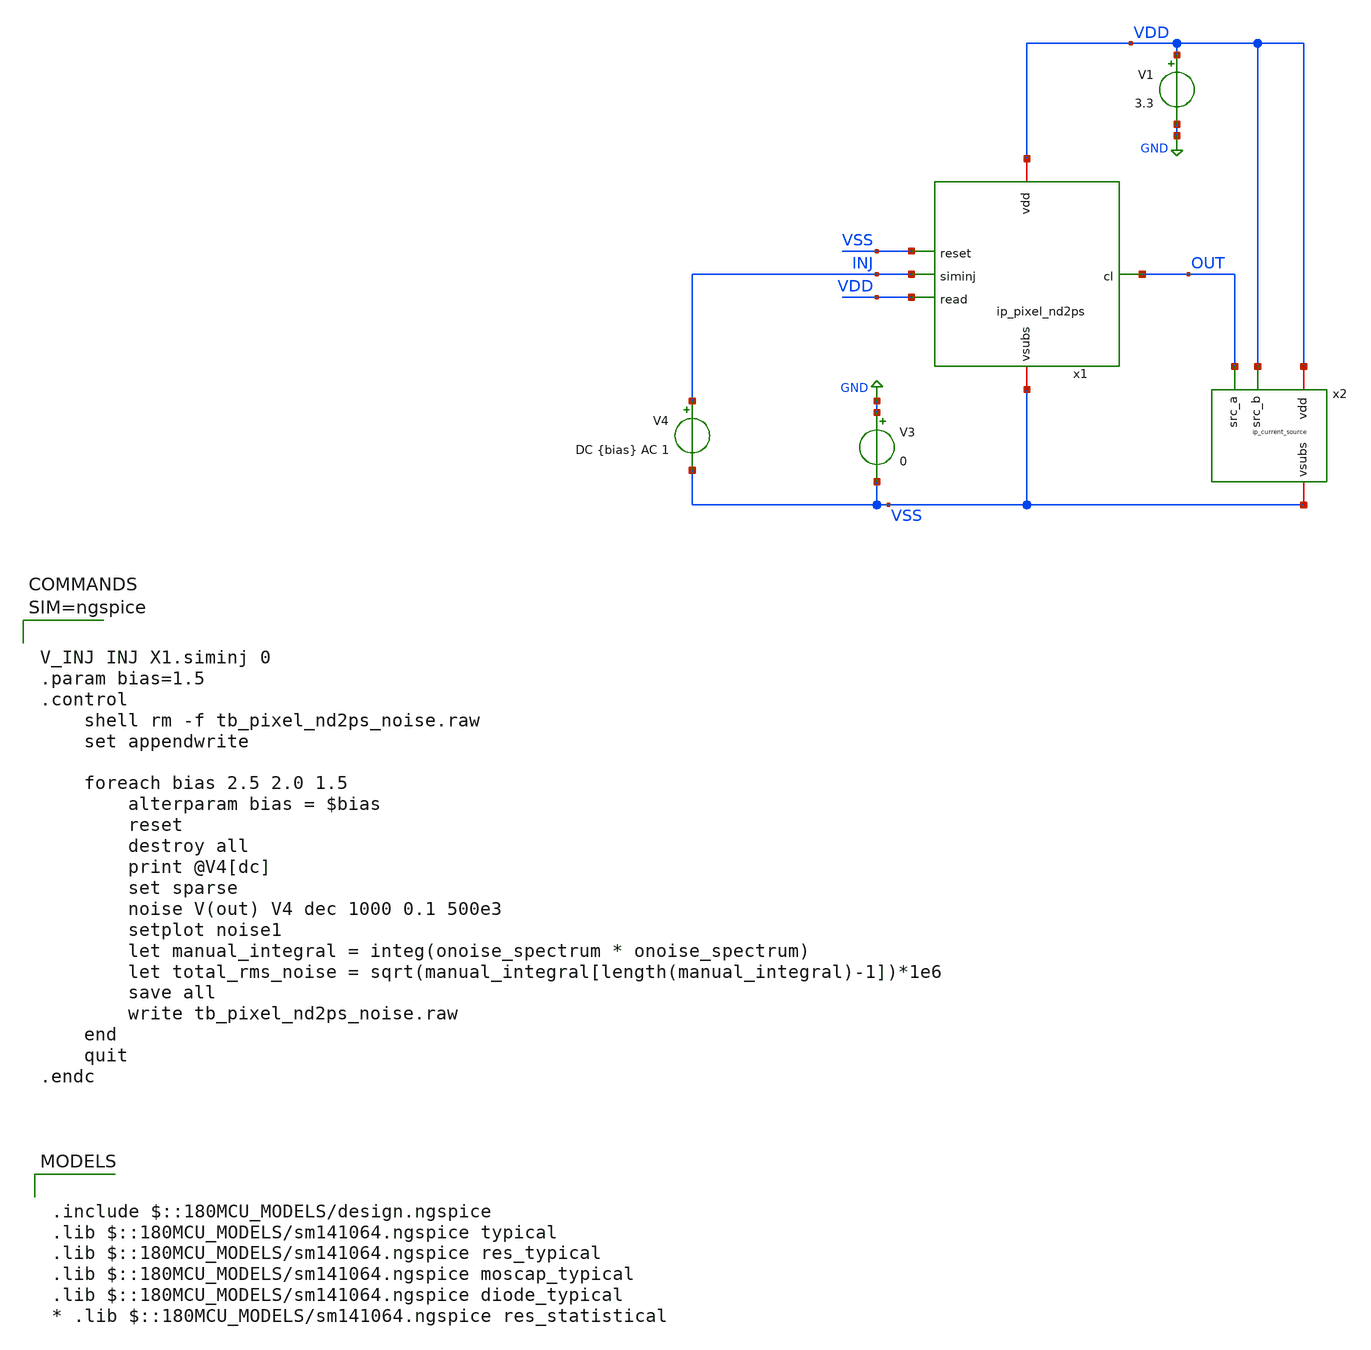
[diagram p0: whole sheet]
** sch_path: xschem/tb_pixel_nd2ps_noise.sch
**.subckt tb_pixel_nd2ps_noise
V1 VDD GND 3.3
V3 GND VSS 0
x1 VDD VSS INJ VDD VSS OUT ip_pixel_nd2ps
V4 INJ VSS DC {bias} AC 1
x2 VDD OUT VSS VDD ip_current_source
**** begin user architecture code

.include $::180MCU_MODELS/design.ngspice
.lib $::180MCU_MODELS/sm141064.ngspice typical
.lib $::180MCU_MODELS/sm141064.ngspice res_typical
.lib $::180MCU_MODELS/sm141064.ngspice moscap_typical
.lib $::180MCU_MODELS/sm141064.ngspice diode_typical
* .lib $::180MCU_MODELS/sm141064.ngspice res_statistical




V_INJ INJ X1.siminj 0
.param bias=1.5
.control
	shell rm -f tb_pixel_nd2ps_noise.raw
	set appendwrite

	foreach bias 2.5 2.0 1.5
		alterparam bias = $bias
		reset
		destroy all
		print @V4[dc]
		set sparse
		noise V(out) V4 dec 1000 0.1 500e3
		setplot noise1
		let manual_integral = integ(onoise_spectrum * onoise_spectrum)
		let total_rms_noise = sqrt(manual_integral[length(manual_integral)-1])*1e6
		save all
		write tb_pixel_nd2ps_noise.raw
	end
	quit
.endc



**** end user architecture code
**.ends

* expanding   symbol:  ip_pixel_nd2ps.sym # of pins=6
** sym_path: xschem/ip_pixel_nd2ps.sym
** sch_path: xschem/ip_pixel_nd2ps.sch
.subckt ip_pixel_nd2ps vdd reset siminj read vsubs cl
*.iopin vdd
*.iopin vsubs
*.ipin siminj
*.ipin reset
*.ipin read
*.opin cl
XM1 vdd reset siminj vsubs nfet_03v3 L=0.3u W=0.3u nf=1 ad='int((nf+1)/2) * W/nf * 0.18u' as='int((nf+2)/2) * W/nf * 0.18u'
+ pd='2*int((nf+1)/2) * (W/nf + 0.18u)' ps='2*int((nf+2)/2) * (W/nf + 0.18u)' nrd='0.18u / W' nrs='0.18u / W'
+ sa=0 sb=0 sd=0 m=1
XM2 vdd siminj sfout vsubs nfet_03v3 L=1u W=2.5u nf=1 ad='int((nf+1)/2) * W/nf * 0.18u' as='int((nf+2)/2) * W/nf * 0.18u'
+ pd='2*int((nf+1)/2) * (W/nf + 0.18u)' ps='2*int((nf+2)/2) * (W/nf + 0.18u)' nrd='0.18u / W' nrs='0.18u / W'
+ sa=0 sb=0 sd=0 m=1
XM3 sfout read cl vsubs nfet_03v3 L=0.3u W=0.3u nf=1 ad='int((nf+1)/2) * W/nf * 0.18u' as='int((nf+2)/2) * W/nf * 0.18u'
+ pd='2*int((nf+1)/2) * (W/nf + 0.18u)' ps='2*int((nf+2)/2) * (W/nf + 0.18u)' nrd='0.18u / W' nrs='0.18u / W'
+ sa=0 sb=0 sd=0 m=1
D1 vsubs siminj diode_nd2ps_03v3 area='13.5u * 13.5u ' pj='2*13.5u + 2*13.5u ' m=1
.ends


* expanding   symbol:  ip_current_source.sym # of pins=4
** sym_path: xschem/ip_current_source.sym
** sch_path: xschem/ip_current_source.sch
.subckt ip_current_source vdd src_a vsubs src_b
*.iopin vdd
*.iopin vsubs
*.ipin src_a
*.ipin src_b
XM8 refin refin vsubs vsubs nfet_06v0 L=1u W=5u nf=1 ad='int((nf+1)/2) * W/nf * 0.18u' as='int((nf+2)/2) * W/nf * 0.18u'
+ pd='2*int((nf+1)/2) * (W/nf + 0.18u)' ps='2*int((nf+2)/2) * (W/nf + 0.18u)' nrd='0.18u / W' nrs='0.18u / W'
+ sa=0 sb=0 sd=0 m=1 par=1
XM5 src_a refin net1 vsubs nfet_06v0 L=0.7u W=5u nf=1 ad='int((nf+1)/2) * W/nf * 0.18u' as='int((nf+2)/2) * W/nf * 0.18u'
+ pd='2*int((nf+1)/2) * (W/nf + 0.18u)' ps='2*int((nf+2)/2) * (W/nf + 0.18u)' nrd='0.18u / W' nrs='0.18u / W'
+ sa=0 sb=0 sd=0 m=2 par=2
XM3 src_b refin net2 vsubs nfet_06v0 L=0.7u W=5u nf=1 ad='int((nf+1)/2) * W/nf * 0.18u' as='int((nf+2)/2) * W/nf * 0.18u'
+ pd='2*int((nf+1)/2) * (W/nf + 0.18u)' ps='2*int((nf+2)/2) * (W/nf + 0.18u)' nrd='0.18u / W' nrs='0.18u / W'
+ sa=0 sb=0 sd=0 m=2 par=2
XM4 net1 refin vsubs vsubs nfet_06v0 L=5u W=0.5u nf=1 ad='int((nf+1)/2) * W/nf * 0.18u' as='int((nf+2)/2) * W/nf * 0.18u'
+ pd='2*int((nf+1)/2) * (W/nf + 0.18u)' ps='2*int((nf+2)/2) * (W/nf + 0.18u)' nrd='0.18u / W' nrs='0.18u / W'
+ sa=0 sb=0 sd=0 m=1 par=1
XM7 net2 refin vsubs vsubs nfet_06v0 L=5u W=0.5u nf=1 ad='int((nf+1)/2) * W/nf * 0.18u' as='int((nf+2)/2) * W/nf * 0.18u'
+ pd='2*int((nf+1)/2) * (W/nf + 0.18u)' ps='2*int((nf+2)/2) * (W/nf + 0.18u)' nrd='0.18u / W' nrs='0.18u / W'
+ sa=0 sb=0 sd=0 m=1 par=1
XR5 refin vdd vsubs ppolyf_u_1k_6p0 r_width=1e-6 r_length=42e-6 m=1
.ends

.GLOBAL GND
.end
